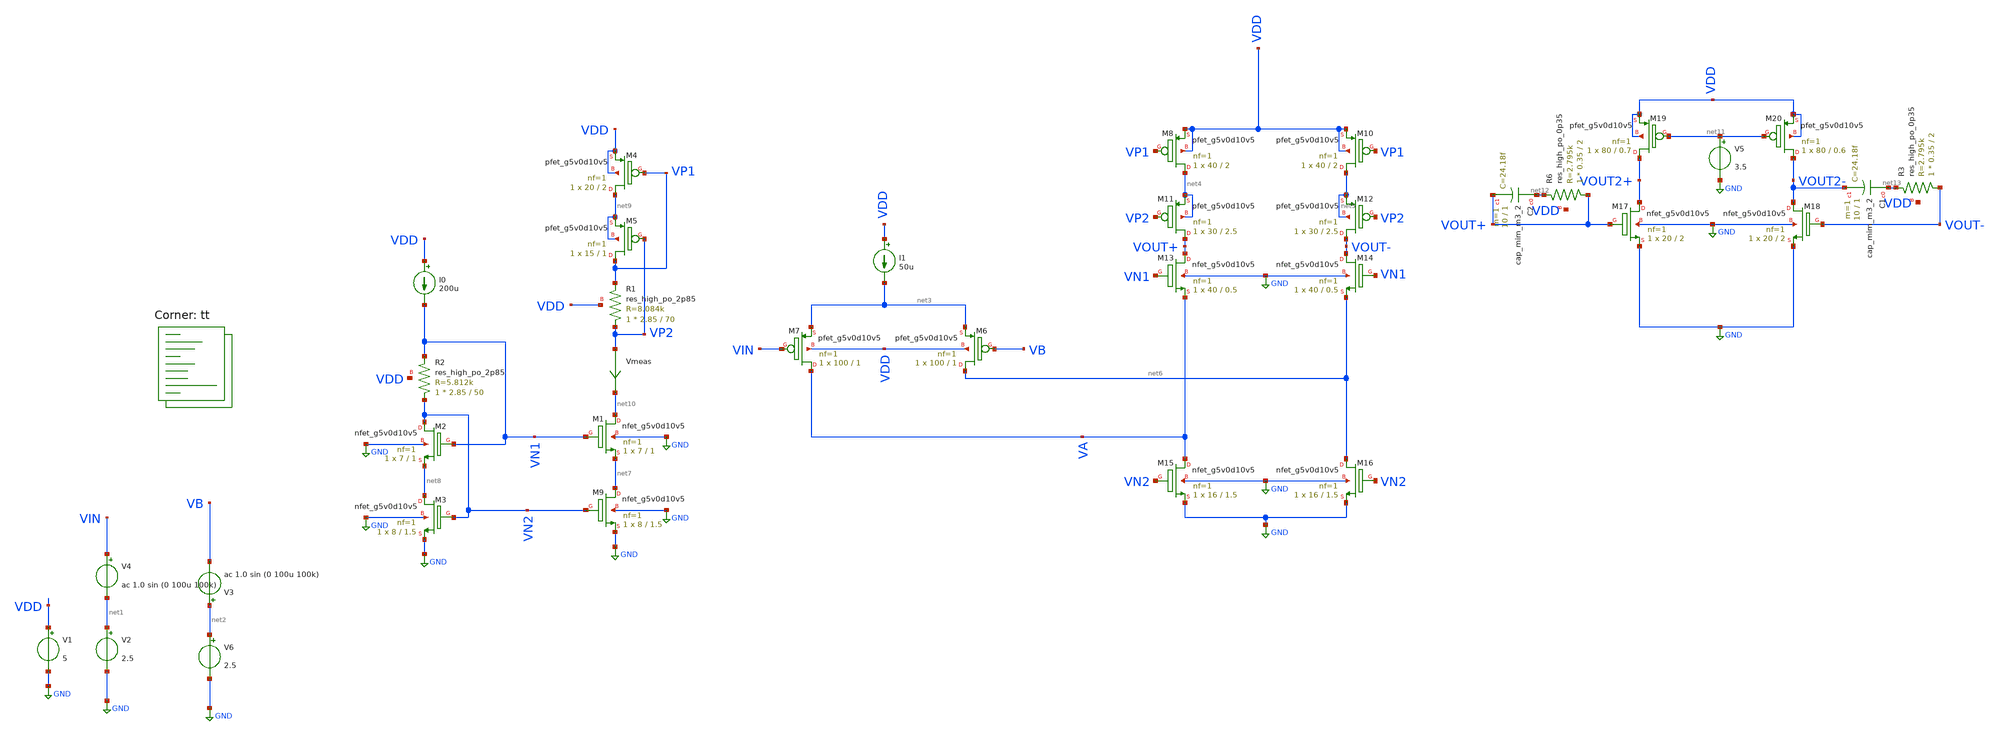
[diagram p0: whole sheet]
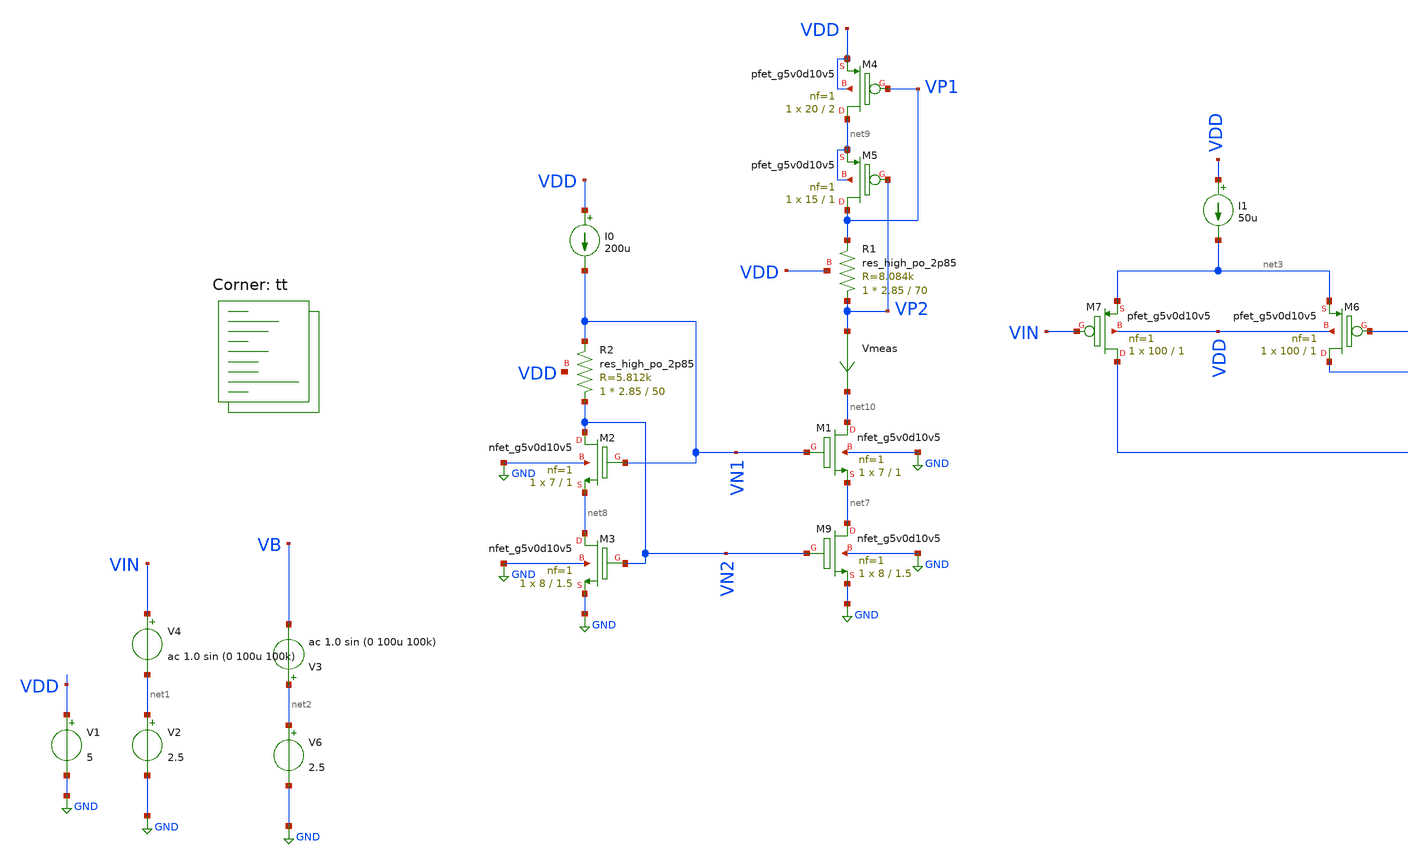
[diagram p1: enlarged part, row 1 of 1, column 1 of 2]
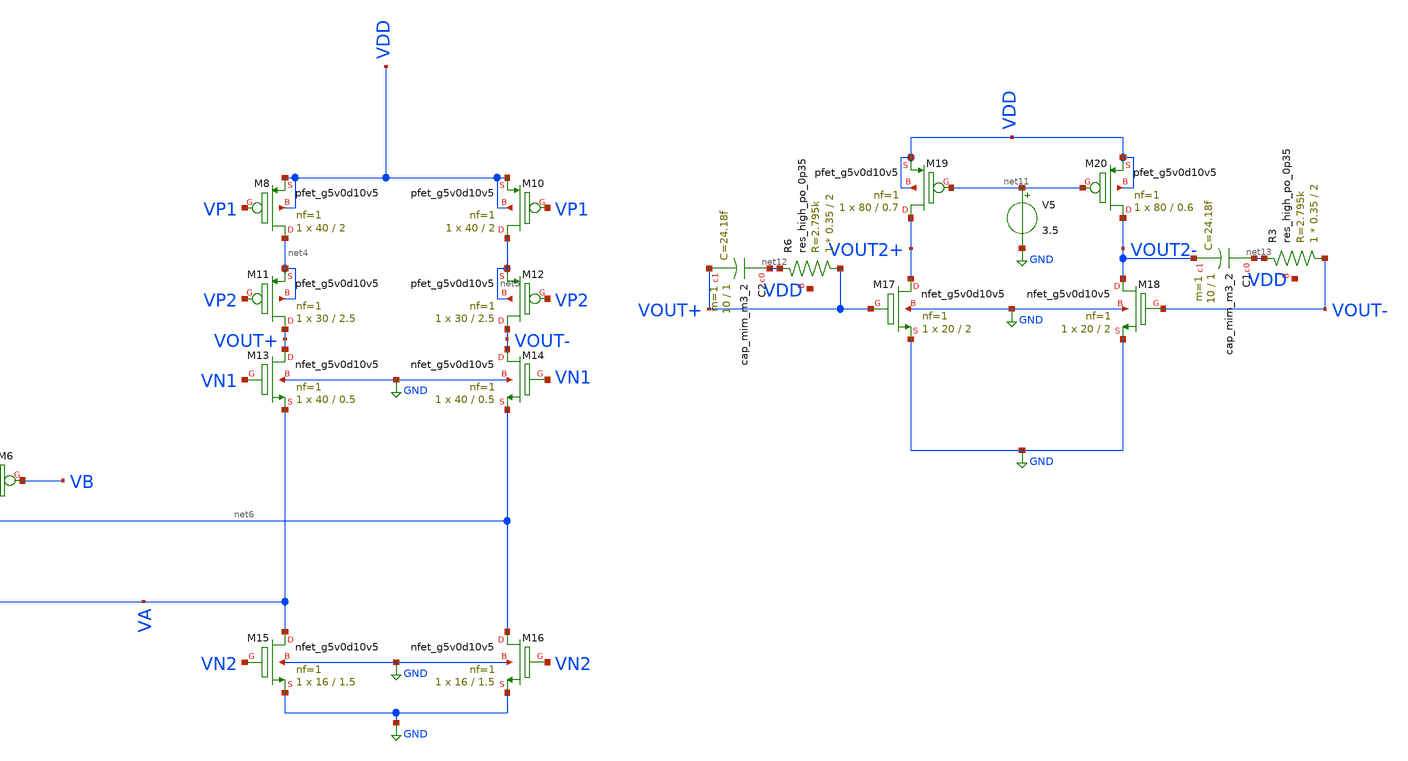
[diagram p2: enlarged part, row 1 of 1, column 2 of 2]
** sch_path: my_amp_test/differential_stage/folded_cascode_diff_stage_test.sch
**.subckt folded_cascode_diff_stage_test
V1 VDD GND 5
V2 net1 GND 2.5
V6 net2 GND 2.5
XM6 net6 VB net3 VDD sky130_fd_pr__pfet_g5v0d10v5 L=1 W=100 nf=1 ad='int((1 + 1)/2) * 100 / 1 * 0.29'
+ as='int((1 + 2)/2) * 100 / 1 * 0.29' pd='2*int((1 + 1)/2) * (100 / 1 + 0.29)' ps='2*int((1 + 2)/2) * (100 / 1 + 0.29)'
+ nrd='0.29 / 100 ' nrs='0.29 / 100 ' sa=0 sb=0 sd=0 mult=1 m=1
XM7 VA VIN net3 VDD sky130_fd_pr__pfet_g5v0d10v5 L=1 W=100 nf=1 ad='int((1 + 1)/2) * 100 / 1 * 0.29'
+ as='int((1 + 2)/2) * 100 / 1 * 0.29' pd='2*int((1 + 1)/2) * (100 / 1 + 0.29)' ps='2*int((1 + 2)/2) * (100 / 1 + 0.29)'
+ nrd='0.29 / 100 ' nrs='0.29 / 100 ' sa=0 sb=0 sd=0 mult=1 m=1
I1 VDD net3 50u
V4 VIN net1 ac 1.0 sin (0 100u 100k)
V3 net2 VB ac 1.0 sin (0 100u 100k)
I0 VDD VN1 200u
XR2 VN2 VN1 VDD sky130_fd_pr__res_high_po_2p85 L=50 mult=1 m=1
XM2 VN2 VN1 net8 GND sky130_fd_pr__nfet_g5v0d10v5 L=1 W=7 nf=1 ad='int((1 + 1)/2) * 7 / 1 * 0.29' as='int((1 + 2)/2) * 7 / 1 * 0.29'
+ pd='2*int((1 + 1)/2) * (7 / 1 + 0.29)' ps='2*int((1 + 2)/2) * (7 / 1 + 0.29)' nrd='0.29 / 7 ' nrs='0.29 / 7 '
+ sa=0 sb=0 sd=0 mult=1 m=1
XM3 net8 VN2 GND GND sky130_fd_pr__nfet_g5v0d10v5 L=1.5 W=8 nf=1 ad='int((1 + 1)/2) * 8 / 1 * 0.29' as='int((1 + 2)/2) * 8 / 1 * 0.29'
+ pd='2*int((1 + 1)/2) * (8 / 1 + 0.29)' ps='2*int((1 + 2)/2) * (8 / 1 + 0.29)' nrd='0.29 / 8 ' nrs='0.29 / 8 '
+ sa=0 sb=0 sd=0 mult=1 m=1
XM4 net9 VP1 VDD VDD sky130_fd_pr__pfet_g5v0d10v5 L=2 W=20 nf=1 ad='int((1 + 1)/2) * 20 / 1 * 0.29' as='int((1 + 2)/2) * 20 / 1 * 0.29'
+ pd='2*int((1 + 1)/2) * (20 / 1 + 0.29)' ps='2*int((1 + 2)/2) * (20 / 1 + 0.29)' nrd='0.29 / 20 ' nrs='0.29 / 20 '
+ sa=0 sb=0 sd=0 mult=1 m=1
XM5 VP1 VP2 net9 net9 sky130_fd_pr__pfet_g5v0d10v5 L=1 W=15 nf=1 ad='int((1 + 1)/2) * 15 / 1 * 0.29'
+ as='int((1 + 2)/2) * 15 / 1 * 0.29' pd='2*int((1 + 1)/2) * (15 / 1 + 0.29)' ps='2*int((1 + 2)/2) * (15 / 1 + 0.29)'
+ nrd='0.29 / 15 ' nrs='0.29 / 15 ' sa=0 sb=0 sd=0 mult=1 m=1
XR1 VP2 VP1 VDD sky130_fd_pr__res_high_po_2p85 L=70 mult=1 m=1
Vmeas VP2 net10 0
.save i(vmeas)
XM1 net10 VN1 net7 GND sky130_fd_pr__nfet_g5v0d10v5 L=1 W=7 nf=1 ad='int((1 + 1)/2) * 7 / 1 * 0.29' as='int((1 + 2)/2) * 7 / 1 * 0.29'
+ pd='2*int((1 + 1)/2) * (7 / 1 + 0.29)' ps='2*int((1 + 2)/2) * (7 / 1 + 0.29)' nrd='0.29 / 7 ' nrs='0.29 / 7 '
+ sa=0 sb=0 sd=0 mult=1 m=1
XM9 net7 VN2 GND GND sky130_fd_pr__nfet_g5v0d10v5 L=1.5 W=8 nf=1 ad='int((1 + 1)/2) * 8 / 1 * 0.29' as='int((1 + 2)/2) * 8 / 1 * 0.29'
+ pd='2*int((1 + 1)/2) * (8 / 1 + 0.29)' ps='2*int((1 + 2)/2) * (8 / 1 + 0.29)' nrd='0.29 / 8 ' nrs='0.29 / 8 '
+ sa=0 sb=0 sd=0 mult=1 m=1
XM8 net4 VP1 VDD VDD sky130_fd_pr__pfet_g5v0d10v5 L=2 W=40 nf=1 ad='int((1 + 1)/2) * 40 / 1 * 0.29' as='int((1 + 2)/2) * 40 / 1 * 0.29'
+ pd='2*int((1 + 1)/2) * (40 / 1 + 0.29)' ps='2*int((1 + 2)/2) * (40 / 1 + 0.29)' nrd='0.29 / 40 ' nrs='0.29 / 40 '
+ sa=0 sb=0 sd=0 mult=1 m=1
XM11 VOUT+ VP2 net4 net4 sky130_fd_pr__pfet_g5v0d10v5 L=2.5 W=30 nf=1 ad='int((1 + 1)/2) * 30 / 1 * 0.29'
+ as='int((1 + 2)/2) * 30 / 1 * 0.29' pd='2*int((1 + 1)/2) * (30 / 1 + 0.29)' ps='2*int((1 + 2)/2) * (30 / 1 + 0.29)'
+ nrd='0.29 / 30 ' nrs='0.29 / 30 ' sa=0 sb=0 sd=0 mult=1 m=1
XM10 net5 VP1 VDD VDD sky130_fd_pr__pfet_g5v0d10v5 L=2 W=40 nf=1 ad='int((1 + 1)/2) * 40 / 1 * 0.29'
+ as='int((1 + 2)/2) * 40 / 1 * 0.29' pd='2*int((1 + 1)/2) * (40 / 1 + 0.29)' ps='2*int((1 + 2)/2) * (40 / 1 + 0.29)'
+ nrd='0.29 / 40 ' nrs='0.29 / 40 ' sa=0 sb=0 sd=0 mult=1 m=1
XM12 VOUT- VP2 net5 net5 sky130_fd_pr__pfet_g5v0d10v5 L=2.5 W=30 nf=1 ad='int((1 + 1)/2) * 30 / 1 * 0.29'
+ as='int((1 + 2)/2) * 30 / 1 * 0.29' pd='2*int((1 + 1)/2) * (30 / 1 + 0.29)' ps='2*int((1 + 2)/2) * (30 / 1 + 0.29)'
+ nrd='0.29 / 30 ' nrs='0.29 / 30 ' sa=0 sb=0 sd=0 mult=1 m=1
XM13 VOUT+ VN1 VA GND sky130_fd_pr__nfet_g5v0d10v5 L=0.5 W=40 nf=1 ad='int((1 + 1)/2) * 40 / 1 * 0.29'
+ as='int((1 + 2)/2) * 40 / 1 * 0.29' pd='2*int((1 + 1)/2) * (40 / 1 + 0.29)' ps='2*int((1 + 2)/2) * (40 / 1 + 0.29)'
+ nrd='0.29 / 40 ' nrs='0.29 / 40 ' sa=0 sb=0 sd=0 mult=1 m=1
XM14 VOUT- VN1 net6 GND sky130_fd_pr__nfet_g5v0d10v5 L=0.5 W=40 nf=1 ad='int((1 + 1)/2) * 40 / 1 * 0.29'
+ as='int((1 + 2)/2) * 40 / 1 * 0.29' pd='2*int((1 + 1)/2) * (40 / 1 + 0.29)' ps='2*int((1 + 2)/2) * (40 / 1 + 0.29)'
+ nrd='0.29 / 40 ' nrs='0.29 / 40 ' sa=0 sb=0 sd=0 mult=1 m=1
XM15 VA VN2 GND GND sky130_fd_pr__nfet_g5v0d10v5 L=1.5 W=16 nf=1 ad='int((1 + 1)/2) * 16 / 1 * 0.29'
+ as='int((1 + 2)/2) * 16 / 1 * 0.29' pd='2*int((1 + 1)/2) * (16 / 1 + 0.29)' ps='2*int((1 + 2)/2) * (16 / 1 + 0.29)'
+ nrd='0.29 / 16 ' nrs='0.29 / 16 ' sa=0 sb=0 sd=0 mult=1 m=1
XM16 net6 VN2 GND GND sky130_fd_pr__nfet_g5v0d10v5 L=1.5 W=16 nf=1 ad='int((1 + 1)/2) * 16 / 1 * 0.29'
+ as='int((1 + 2)/2) * 16 / 1 * 0.29' pd='2*int((1 + 1)/2) * (16 / 1 + 0.29)' ps='2*int((1 + 2)/2) * (16 / 1 + 0.29)'
+ nrd='0.29 / 16 ' nrs='0.29 / 16 ' sa=0 sb=0 sd=0 mult=1 m=1
XM17 VOUT2+ VOUT+ GND GND sky130_fd_pr__nfet_g5v0d10v5 L=2 W=20 nf=1 ad='int((1 + 1)/2) * 20 / 1 * 0.29'
+ as='int((1 + 2)/2) * 20 / 1 * 0.29' pd='2*int((1 + 1)/2) * (20 / 1 + 0.29)' ps='2*int((1 + 2)/2) * (20 / 1 + 0.29)'
+ nrd='0.29 / 20 ' nrs='0.29 / 20 ' sa=0 sb=0 sd=0 mult=1 m=1
XM18 VOUT2- VOUT- GND GND sky130_fd_pr__nfet_g5v0d10v5 L=2 W=20 nf=1 ad='int((1 + 1)/2) * 20 / 1 * 0.29'
+ as='int((1 + 2)/2) * 20 / 1 * 0.29' pd='2*int((1 + 1)/2) * (20 / 1 + 0.29)' ps='2*int((1 + 2)/2) * (20 / 1 + 0.29)'
+ nrd='0.29 / 20 ' nrs='0.29 / 20 ' sa=0 sb=0 sd=0 mult=1 m=1
XM19 VOUT2+ net11 VDD VDD sky130_fd_pr__pfet_g5v0d10v5 L=0.7 W=80 nf=1 ad='int((1 + 1)/2) * 80 / 1 * 0.29'
+ as='int((1 + 2)/2) * 80 / 1 * 0.29' pd='2*int((1 + 1)/2) * (80 / 1 + 0.29)' ps='2*int((1 + 2)/2) * (80 / 1 + 0.29)'
+ nrd='0.29 / 80 ' nrs='0.29 / 80 ' sa=0 sb=0 sd=0 mult=1 m=1
XM20 VOUT2- net11 VDD VDD sky130_fd_pr__pfet_g5v0d10v5 L=0.6 W=80 nf=1 ad='int((1 + 1)/2) * 80 / 1 * 0.29'
+ as='int((1 + 2)/2) * 80 / 1 * 0.29' pd='2*int((1 + 1)/2) * (80 / 1 + 0.29)' ps='2*int((1 + 2)/2) * (80 / 1 + 0.29)'
+ nrd='0.29 / 80 ' nrs='0.29 / 80 ' sa=0 sb=0 sd=0 mult=1 m=1
V5 net11 GND 3.5
XC2 net12 VOUT+ sky130_fd_pr__cap_mim_m3_2 W=10 L=1 MF=1 m=1
XR6 VOUT+ net12 VDD sky130_fd_pr__res_high_po_0p35 L=2 mult=1 m=1
XC1 net13 VOUT2- sky130_fd_pr__cap_mim_m3_2 W=10 L=1 MF=1 m=1
XR3 VOUT- net13 VDD sky130_fd_pr__res_high_po_0p35 L=2 mult=1 m=1
**** begin user architecture code

**************************************************************
**************************************************************
**************************************************************
**************************************************************
**************************************************************
*LIBs*********************************************************
**************************************************************
**************************************************************
**************************************************************
**************************************************************
**************************************************************
*.lib $::SKYWATER_MODELS/sky130.lib.spice tt
* chose the corners in the corner file
* tt_mm for mismatch
* ss ff sf fs standart corners
* ll hh lh hl capacitor and resistors corners
* mc for total process variation including corners
**************************************************************
**************************************************************
**************************************************************
**************************************************************
**************************************************************
*Corners/montecarlo options***********************************
**************************************************************
**************************************************************
**************************************************************
**************************************************************
**************************************************************
.TEMP 27
**************************************************************
**************************************************************
**************************************************************
**************************************************************
*SIMULATION and Plots*****************************************
**************************************************************
**************************************************************
**************************************************************
**************************************************************
.control
save all
dc V2 0 5 0.001
plot v(VOUT+) v(VOUT-) deriv(v(VOUT+)) deriv(v(VOUT-))
plot v(VOUT2+) v(VOUT2-) deriv(v(VOUT2+)) deriv(v(VOUT2-))
*plot v(VA)
*plot i(Vmeas)
ac dec 20 1 1000G
plot db(v(VOUT+))
plot db(v(VOUT2+)) phase(v(VOUT+))
.endc

.lib $::SKYWATER_MODELS/sky130.lib.spice tt
**** end user architecture code
**.ends
.GLOBAL GND
.end
